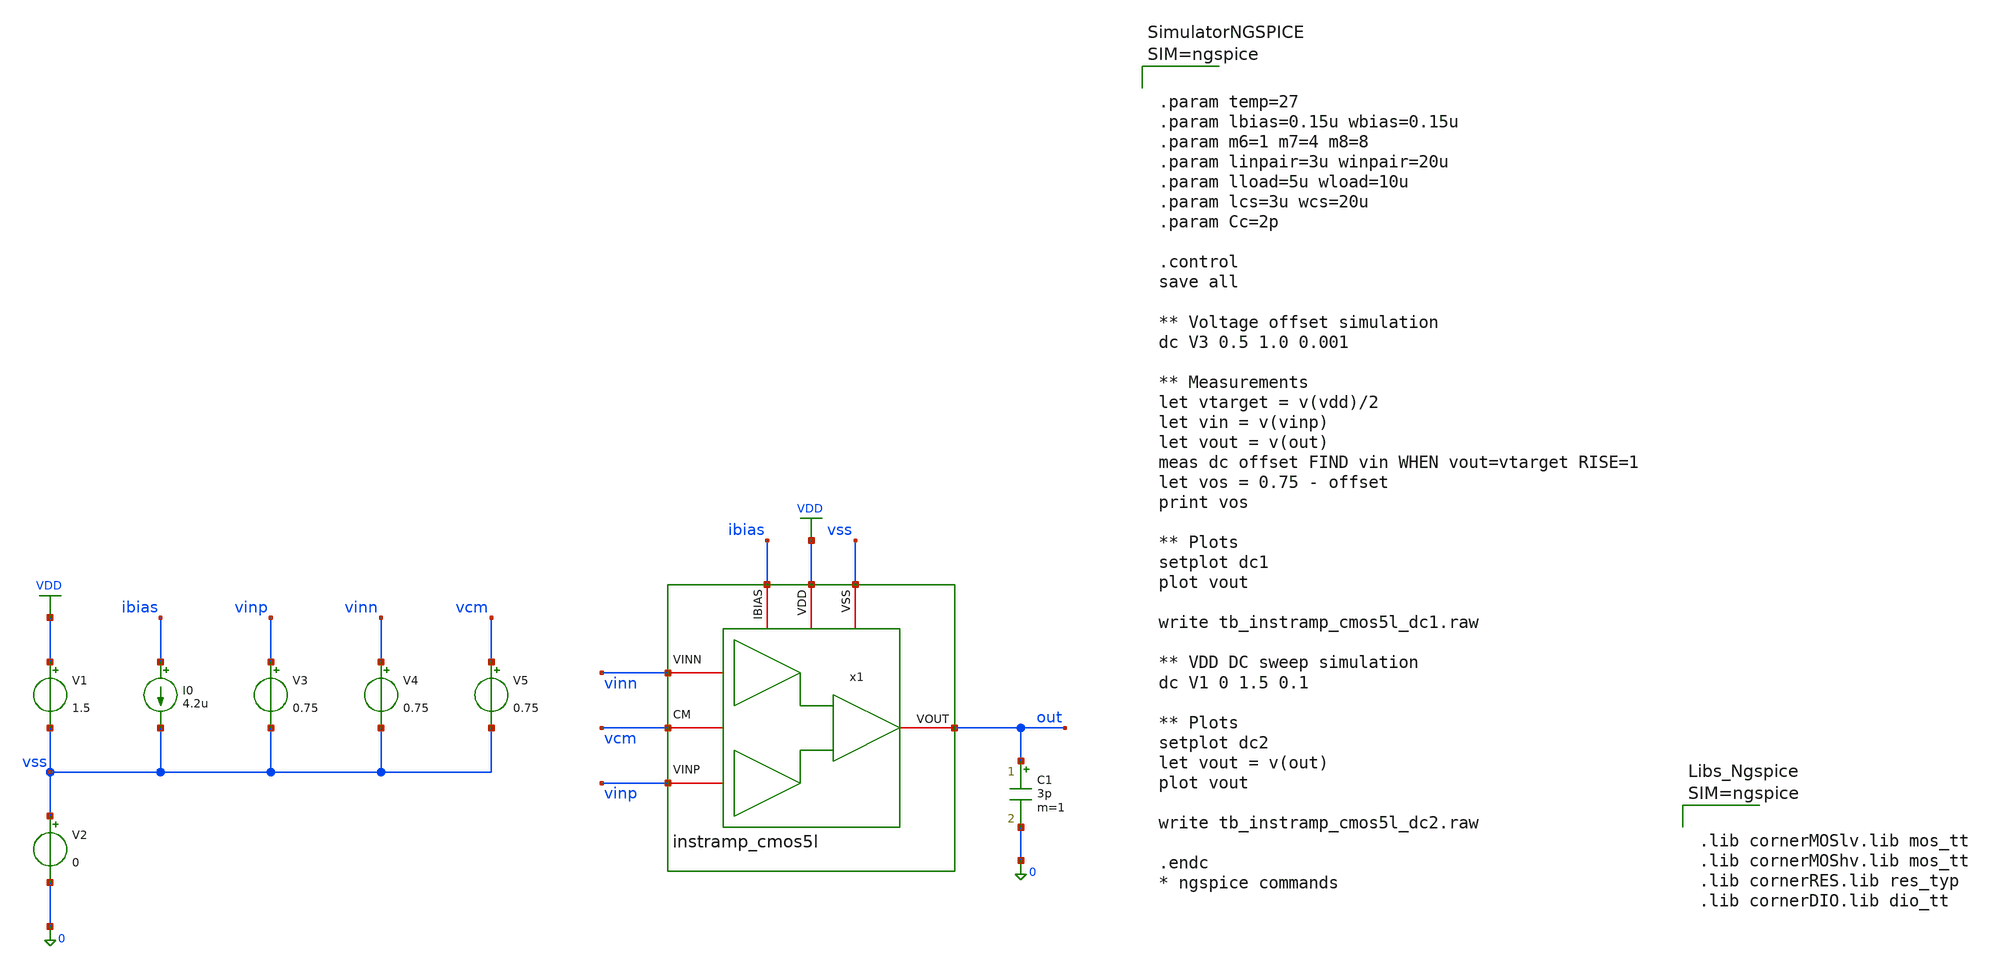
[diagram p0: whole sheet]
** sch_path: designs/libs/tb_analog/tb_instramp_cmos5l_dc/tb_instramp_cmos5l_dc.sch
**.subckt tb_instramp_cmos5l_dc
C1 out 0 3p m=1
I0 ibias vss 4.2u
V1 VDD vss 1.5
V2 vss 0 0
V3 vinp vss 0.75
V4 vinn vss 0.75
x1 vss VDD ibias vinn out vinp vcm instramp_cmos5l
V5 vcm vss 0.75
**** begin user architecture code



.param temp=27
.param lbias=0.15u wbias=0.15u
.param m6=1 m7=4 m8=8
.param linpair=3u winpair=20u
.param lload=5u wload=10u
.param lcs=3u wcs=20u
.param Cc=2p

.control
save all

** Voltage offset simulation
dc V3 0.5 1.0 0.001

** Measurements
let vtarget = v(vdd)/2
let vin = v(vinp)
let vout = v(out)
meas dc offset FIND vin WHEN vout=vtarget RISE=1
let vos = 0.75 - offset
print vos

** Plots
setplot dc1
plot vout

write tb_instramp_cmos5l_dc1.raw

** VDD DC sweep simulation
dc V1 0 1.5 0.1

** Plots
setplot dc2
let vout = v(out)
plot vout

write tb_instramp_cmos5l_dc2.raw

.endc
* ngspice commands






.lib cornerMOSlv.lib mos_tt
.lib cornerMOShv.lib mos_tt
.lib cornerRES.lib res_typ
.lib cornerDIO.lib dio_tt



**** end user architecture code
**.ends

* expanding   symbol:
*+  /foss/designs/Programmable-Instrumentation-Amplifier-IP/designs/libs/core_analog/instramp_cmos5l/instramp_cmos5l.sym # of pins=7
** sym_path: designs/libs/core_analog/instramp_cmos5l/instramp_cmos5l.sym
** sch_path: designs/libs/core_analog/instramp_cmos5l/instramp_cmos5l.sch
.subckt instramp_cmos5l VSS VDD IBIAS VINN VOUT VINP CM
*.iopin VDD
*.iopin IBIAS
*.iopin VSS
*.iopin CM
*.iopin VOUT
*.iopin VINN
*.iopin VINP
x1 vss ibias vdd net3 VINP net4 ota_cmos5l
x2 vss ibias vdd net1 VINN net2 ota_cmos5l
x3 vss ibias vdd net5 net6 net8 ota_cmos5l
XR1 net4 net6 sub! rhigh w=0.5e-6 l=2e-6 m=1 b=0 mm_ok=1
XR2 net2 net5 sub! rhigh w=0.5e-6 l=2e-6 m=1 b=0 mm_ok=1
XR3 net6 CM sub! rhigh w=0.5e-6 l=8*2.1e-6 m=1 b=0 mm_ok=1
XR4 net5 net7 sub! rhigh w=0.5e-6 l=8*2.1e-6 m=1 b=0 mm_ok=1
Vmeas net7 net8 0
.save i(vmeas)
Vmeas1 net8 VOUT 0
.save i(vmeas1)
R5 VINN vcm 10MEG m=1
R6 vcm VINP 10MEG m=1
XR7 net2 net1 sub! rhigh w=0.5e-6 l=2e-6 m=1 b=0 mm_ok=1
XR8 net4 net3 sub! rhigh w=0.5e-6 l=2e-6 m=1 b=0 mm_ok=1
.ends


* expanding   symbol:
*+  /foss/designs/Programmable-Instrumentation-Amplifier-IP/designs/libs/core_analog/ota_cmos5l/ota_cmos5l.sym # of pins=6
** sym_path: /foss/designs/Programmable-Instrumentation-Amplifier-IP/designs/libs/core_analog/ota_cmos5l/ota_cmos5l.sym
** sch_path: /foss/designs/Programmable-Instrumentation-Amplifier-IP/designs/libs/core_analog/ota_cmos5l/ota_cmos5l.sch
.subckt ota_cmos5l VSS IBIAS VDD VINN VINP VOUT
*.iopin IBIAS
*.iopin VDD
*.iopin VSS
*.iopin VOUT
*.iopin VINP
*.iopin VINN
XM6 net1 net1 vdd vdd sg13_lv_pmos w={wbias} l={lbias} ng=1 m={m6} mm_ok=1
XM7 net5 net1 vdd vdd sg13_lv_pmos w={wbias} l={lbias} ng=1 m={m7} mm_ok=1
XM8 net6 net1 vdd vdd sg13_lv_pmos w={wbias} l={lbias} ng=1 m={m8} mm_ok=1
XM1 net7 VINN net2 vdd sg13_lv_pmos w={winpair} l={linpair} ng=1 m=1 mm_ok=1
XM2 net8 VINP net2 vdd sg13_lv_pmos w={winpair} l={linpair} ng=1 m=1 mm_ok=1
XM3 net3 net3 gnd gnd sg13_lv_nmos w={wload} l={lload} ng=1 m=1 mm_ok=1
XM4 net4 net3 gnd gnd sg13_lv_nmos w={wload} l={lload} ng=1 m=1 mm_ok=1
XM5 net9 net4 gnd gnd sg13_lv_nmos w={wcs} l={lcs} ng=1 m=1 mm_ok=1
C1 net10 net9 {Cc} m=1
XR1 net4 net10 sub! rhigh w=0.5e-6 l=1.95e-6 m=1 b=0 mm_ok=1
**** begin user architecture code



.include ota_cmos5l.save
.param temp=27
.param lbias=0.15u wbias=0.15u
.param m6=1 m7=4 m8=10
.param linpair=3u winpair=20u
.param lload=0.5u wload=0.42u
.param lcs=5u wcs=19.13u
.param Cc=1.5p
.control
op
write ota_cmos5l.raw
.endc



**** end user architecture code
**** begin user architecture code



.lib cornerMOSlv.lib mos_tt
.lib cornerMOShv.lib mos_tt
.lib cornerRES.lib res_typ
.lib cornerDIO.lib dio_tt



**** end user architecture code
VIBIAS net1 ibias 0
.save i(vibias)
VID7 net5 net2 0
.save i(vid7)
VID8 net6 VOUT 0
.save i(vid8)
VIVDD VDD vdd 0
.save i(vivdd)
.save v(vinp)
.save v(vinn)
.save v(vout)
VID1 net7 net3 0
.save i(vid1)
VID2 net8 net4 0
.save i(vid2)
VID5 VOUT net9 0
.save i(vid5)
.ends

.GLOBAL VDD
.end
